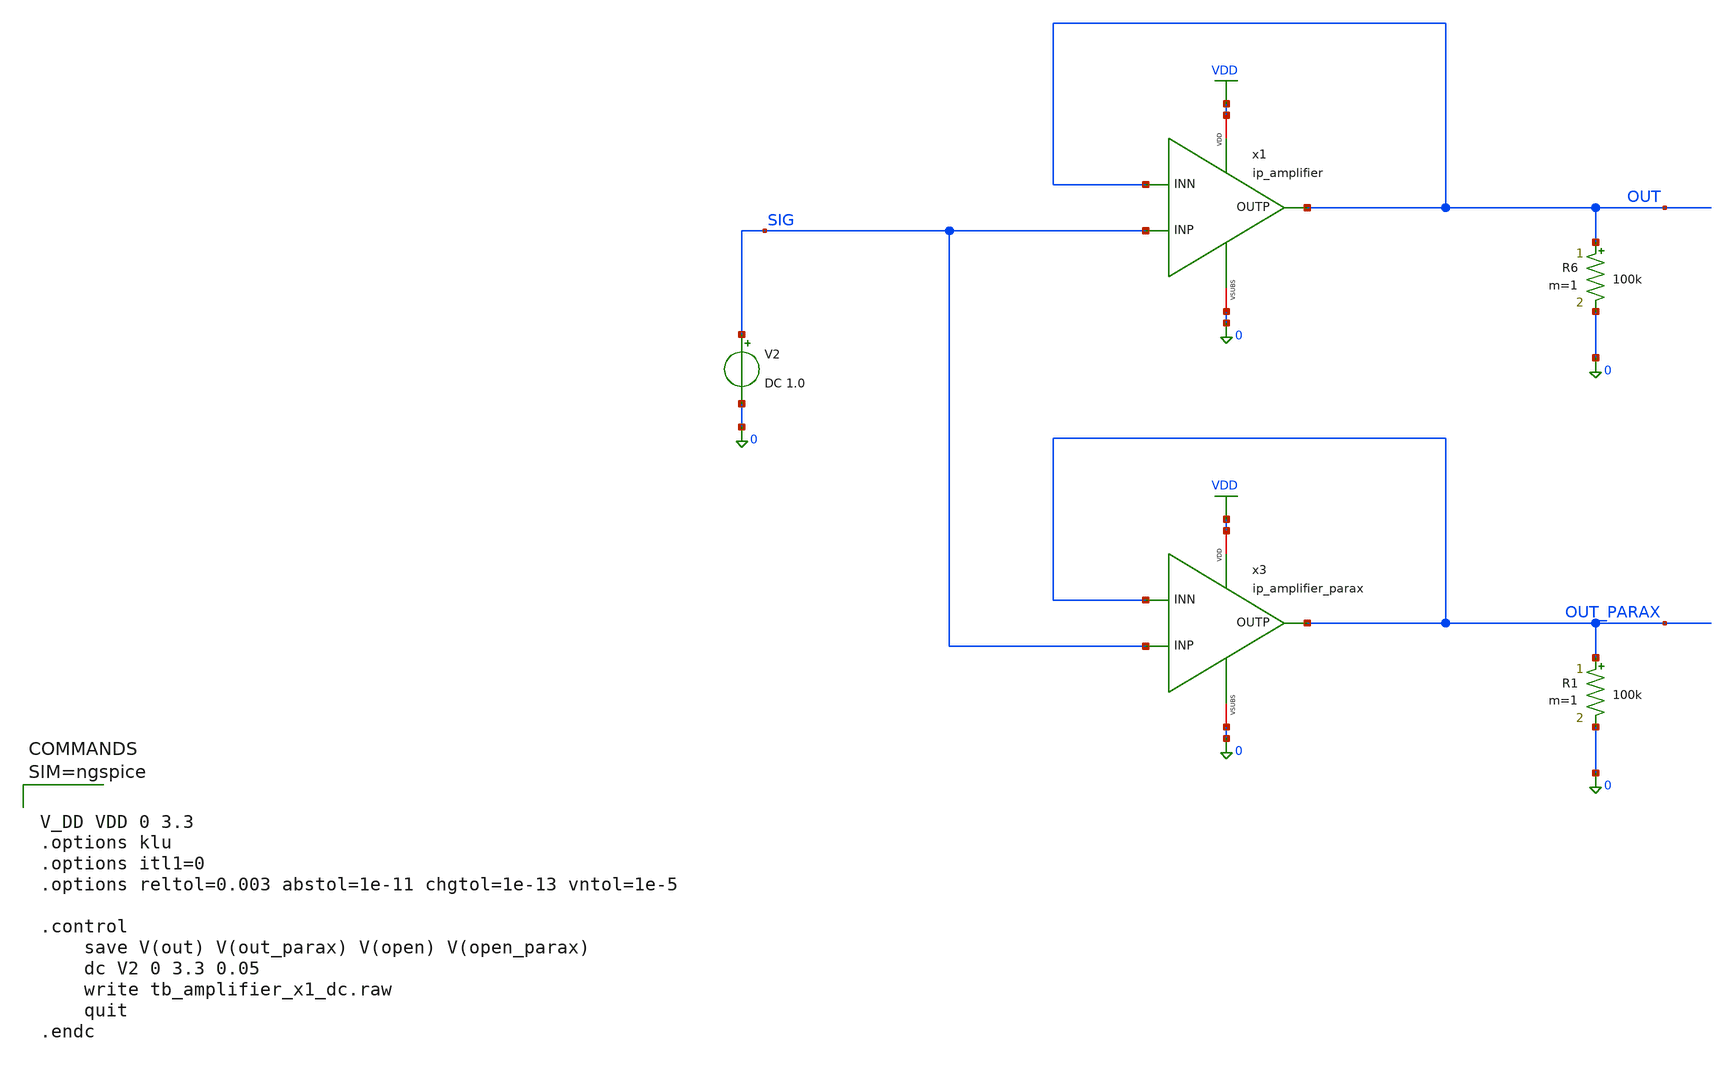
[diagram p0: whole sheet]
** sch_path: analog/xschem/tb_amplifier_x1_dc.sch
**.subckt tb_amplifier_x1_dc
x1 VDD 0 SIG OUT OUT ip_amplifier
R6 OUT 0 100k m=1
V2 SIG 0 DC 1.0
R1 OUT_PARAX 0 100k m=1
x3 VDD 0 SIG OUT_PARAX OUT_PARAX ip_amplifier_parax
**** begin user architecture code

.inc $::180MCU_MODELS/design.spice
.lib $::180MCU_MODELS/sm141064.ngspice typical
.lib $::180MCU_MODELS/sm141064.ngspice cap_mim
.lib $::180MCU_MODELS/sm141064.ngspice moscap_typical
.lib $::180MCU_MODELS/sm141064.ngspice diode_typical
.lib $::180MCU_MODELS/sm141064.ngspice res_typical
.lib $::180MCU_MODELS/sm141064.ngspice mimcap_typical




V_DD VDD 0 3.3
.options klu
.options itl1=0
.options reltol=0.003 abstol=1e-11 chgtol=1e-13 vntol=1e-5

.control
	save V(out) V(out_parax) V(open) V(open_parax)
	dc V2 0 3.3 0.05
	write tb_amplifier_x1_dc.raw
	quit
.endc



**** end user architecture code
**.ends
.GLOBAL VDD
.end
